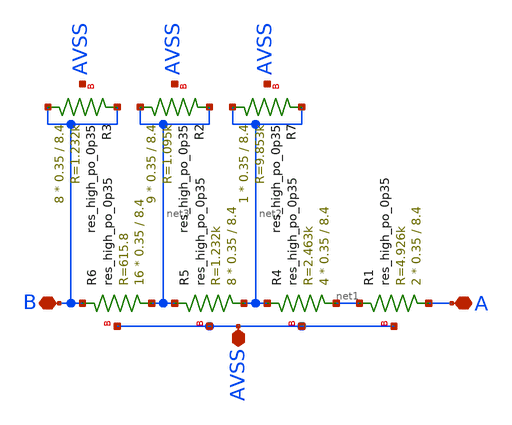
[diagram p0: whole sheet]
** sch_path: magic/res_trim.sch
**.subckt res_trim B A AVSS
*.iopin B
*.iopin A
*.iopin AVSS
XR1 A net1 AVSS sky130_fd_pr__res_high_po_0p35 L=8.4 mult=2 m=2
XR4 net1 net2 AVSS sky130_fd_pr__res_high_po_0p35 L=8.4 mult=4 m=4
XR5 net2 net3 AVSS sky130_fd_pr__res_high_po_0p35 L=8.4 mult=8 m=8
XR6 net3 B AVSS sky130_fd_pr__res_high_po_0p35 L=8.4 mult=16 m=16
XR2 net3 net3 AVSS sky130_fd_pr__res_high_po_0p35 L=8.4 mult=9 m=9
XR3 B B AVSS sky130_fd_pr__res_high_po_0p35 L=8.4 mult=8 m=8
XR7 net2 net2 AVSS sky130_fd_pr__res_high_po_0p35 L=8.4 mult=1 m=1
**.ends
.end
